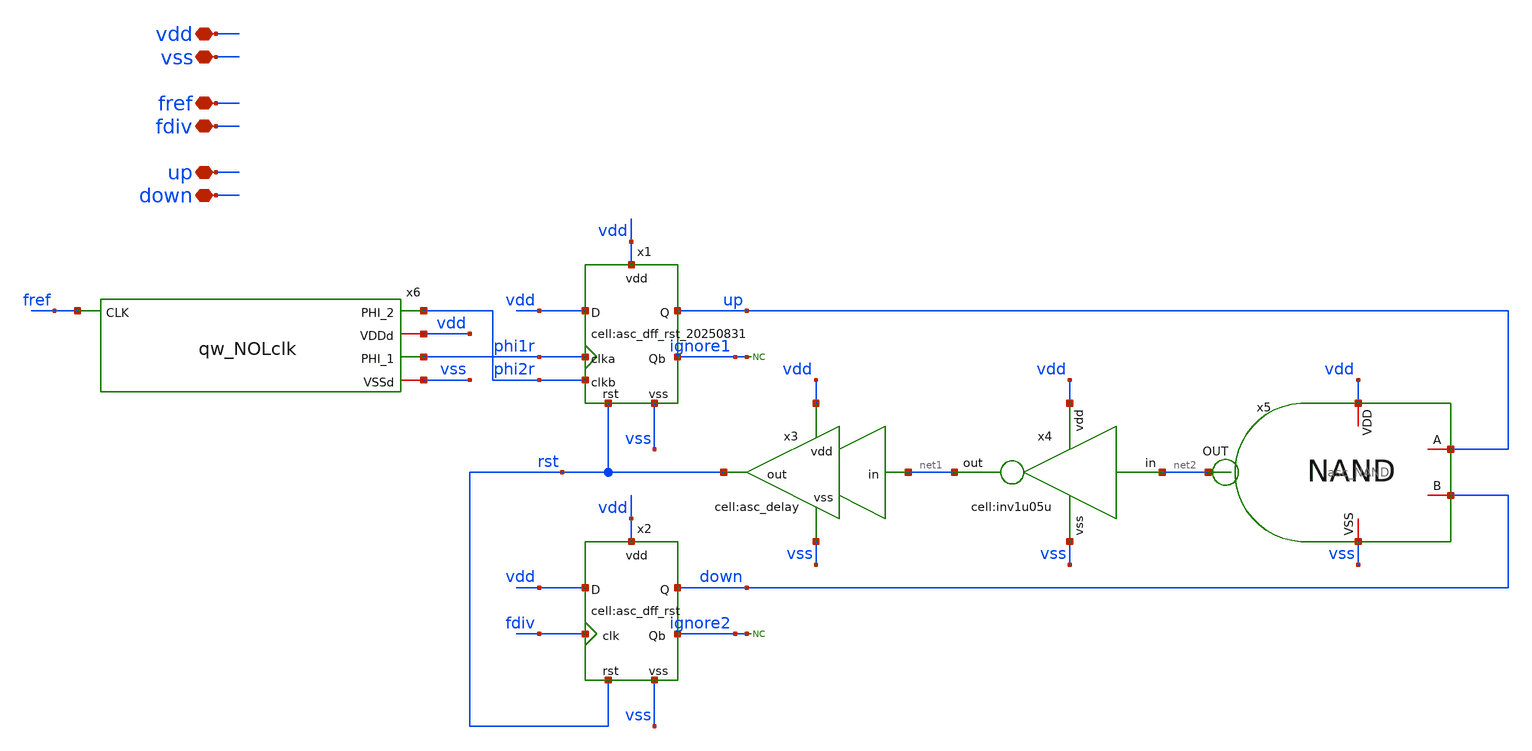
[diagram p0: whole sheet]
** sch_path: designs/libs/core_analog/asc_PFD_DFF_20250831/asc_PFD_DFF_20250831.sch
**.subckt asc_PFD_DFF_20250831 vdd vss fref fdiv up down
*.iopin vdd
*.iopin vss
*.iopin fref
*.iopin fdiv
*.iopin up
*.iopin down
x4 net2 vdd net1 vss inv1u05u
x3 net1 vss rst vdd asc_delay
x5 vdd net2 up down vss asc_NAND
* noconn ignore1
* noconn ignore2
x1 phi1r vdd ignore1 vdd vss up rst phi2r asc_dff_rst_20250831
x6 phi2r fref vdd phi1r vss qw_NOLclk
x2 fdiv vdd ignore2 vdd vss down rst asc_dff_rst
**.ends
.end
